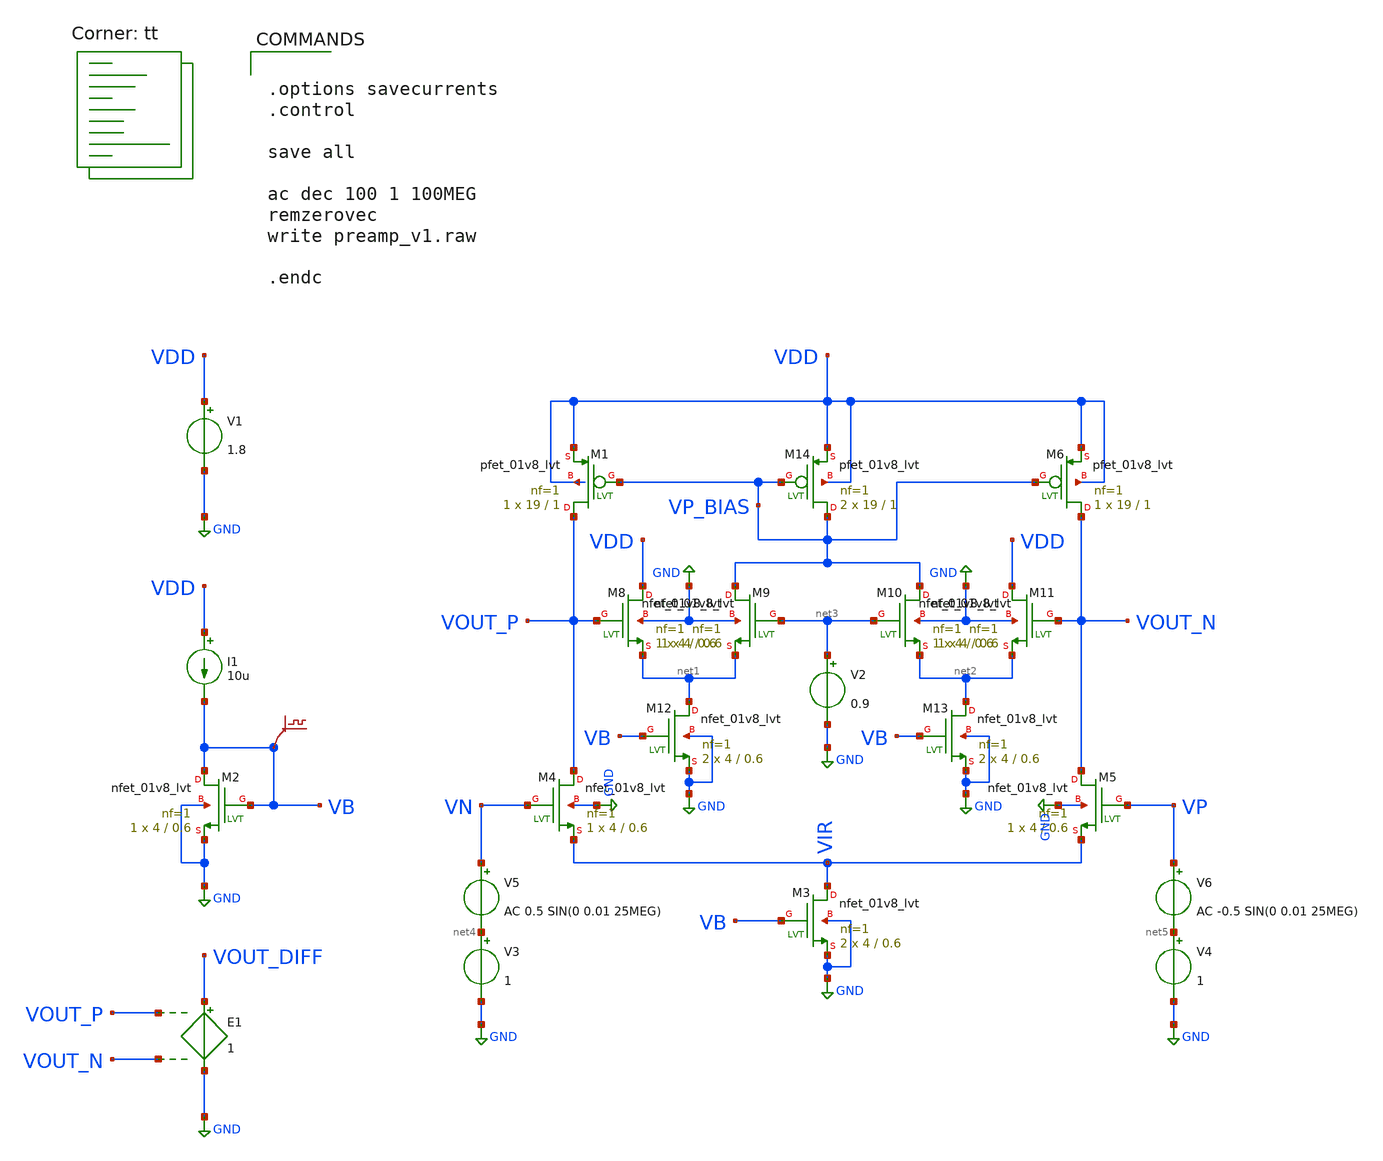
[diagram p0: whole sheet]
** sch_path: strongARM/preamp_v1.sch
**.subckt preamp_v1
V1 VDD GND 1.8
XM2 VB VB GND GND sky130_fd_pr__nfet_01v8_lvt L=0.6 W=4 nf=1 ad='int((nf+1)/2) * W/nf * 0.29' as='int((nf+2)/2) * W/nf * 0.29'
+ pd='2*int((nf+1)/2) * (W/nf + 0.29)' ps='2*int((nf+2)/2) * (W/nf + 0.29)' nrd='0.29 / W' nrs='0.29 / W'
+ sa=0 sb=0 sd=0 mult=1 m=1
I1 VDD VB 10u
XM3 VIR VB GND GND sky130_fd_pr__nfet_01v8_lvt L=0.6 W=4 nf=1 ad='int((nf+1)/2) * W/nf * 0.29' as='int((nf+2)/2) * W/nf * 0.29'
+ pd='2*int((nf+1)/2) * (W/nf + 0.29)' ps='2*int((nf+2)/2) * (W/nf + 0.29)' nrd='0.29 / W' nrs='0.29 / W'
+ sa=0 sb=0 sd=0 mult=2 m=2
XM4 VOUT_P VN VIR GND sky130_fd_pr__nfet_01v8_lvt L=0.6 W=4 nf=1 ad='int((nf+1)/2) * W/nf * 0.29' as='int((nf+2)/2) * W/nf * 0.29'
+ pd='2*int((nf+1)/2) * (W/nf + 0.29)' ps='2*int((nf+2)/2) * (W/nf + 0.29)' nrd='0.29 / W' nrs='0.29 / W'
+ sa=0 sb=0 sd=0 mult=1 m=1
XM5 VOUT_N VP VIR GND sky130_fd_pr__nfet_01v8_lvt L=0.6 W=4 nf=1 ad='int((nf+1)/2) * W/nf * 0.29' as='int((nf+2)/2) * W/nf * 0.29'
+ pd='2*int((nf+1)/2) * (W/nf + 0.29)' ps='2*int((nf+2)/2) * (W/nf + 0.29)' nrd='0.29 / W' nrs='0.29 / W'
+ sa=0 sb=0 sd=0 mult=1 m=1
XM6 VOUT_N VP_BIAS VDD VDD sky130_fd_pr__pfet_01v8_lvt L=1 W=19 nf=1 ad='int((nf+1)/2) * W/nf * 0.29'
+ as='int((nf+2)/2) * W/nf * 0.29' pd='2*int((nf+1)/2) * (W/nf + 0.29)' ps='2*int((nf+2)/2) * (W/nf + 0.29)'
+ nrd='0.29 / W' nrs='0.29 / W' sa=0 sb=0 sd=0 mult=1 m=1
XM8 VDD VOUT_P net1 GND sky130_fd_pr__nfet_01v8_lvt L=0.6 W=4 nf=1 ad='int((nf+1)/2) * W/nf * 0.29' as='int((nf+2)/2) * W/nf * 0.29'
+ pd='2*int((nf+1)/2) * (W/nf + 0.29)' ps='2*int((nf+2)/2) * (W/nf + 0.29)' nrd='0.29 / W' nrs='0.29 / W'
+ sa=0 sb=0 sd=0 mult=1 m=1
XM9 VP_BIAS net3 net1 GND sky130_fd_pr__nfet_01v8_lvt L=0.6 W=4 nf=1 ad='int((nf+1)/2) * W/nf * 0.29'
+ as='int((nf+2)/2) * W/nf * 0.29' pd='2*int((nf+1)/2) * (W/nf + 0.29)' ps='2*int((nf+2)/2) * (W/nf + 0.29)'
+ nrd='0.29 / W' nrs='0.29 / W' sa=0 sb=0 sd=0 mult=1 m=1
XM10 VP_BIAS net3 net2 GND sky130_fd_pr__nfet_01v8_lvt L=0.6 W=4 nf=1 ad='int((nf+1)/2) * W/nf * 0.29'
+ as='int((nf+2)/2) * W/nf * 0.29' pd='2*int((nf+1)/2) * (W/nf + 0.29)' ps='2*int((nf+2)/2) * (W/nf + 0.29)'
+ nrd='0.29 / W' nrs='0.29 / W' sa=0 sb=0 sd=0 mult=1 m=1
XM11 VDD VOUT_N net2 GND sky130_fd_pr__nfet_01v8_lvt L=0.6 W=4 nf=1 ad='int((nf+1)/2) * W/nf * 0.29'
+ as='int((nf+2)/2) * W/nf * 0.29' pd='2*int((nf+1)/2) * (W/nf + 0.29)' ps='2*int((nf+2)/2) * (W/nf + 0.29)'
+ nrd='0.29 / W' nrs='0.29 / W' sa=0 sb=0 sd=0 mult=1 m=1
XM12 net1 VB GND GND sky130_fd_pr__nfet_01v8_lvt L=0.6 W=4 nf=1 ad='int((nf+1)/2) * W/nf * 0.29' as='int((nf+2)/2) * W/nf * 0.29'
+ pd='2*int((nf+1)/2) * (W/nf + 0.29)' ps='2*int((nf+2)/2) * (W/nf + 0.29)' nrd='0.29 / W' nrs='0.29 / W'
+ sa=0 sb=0 sd=0 mult=2 m=2
XM13 net2 VB GND GND sky130_fd_pr__nfet_01v8_lvt L=0.6 W=4 nf=1 ad='int((nf+1)/2) * W/nf * 0.29' as='int((nf+2)/2) * W/nf * 0.29'
+ pd='2*int((nf+1)/2) * (W/nf + 0.29)' ps='2*int((nf+2)/2) * (W/nf + 0.29)' nrd='0.29 / W' nrs='0.29 / W'
+ sa=0 sb=0 sd=0 mult=2 m=2
XM14 VP_BIAS VP_BIAS VDD VDD sky130_fd_pr__pfet_01v8_lvt L=1 W=19 nf=1 ad='int((nf+1)/2) * W/nf * 0.29'
+ as='int((nf+2)/2) * W/nf * 0.29' pd='2*int((nf+1)/2) * (W/nf + 0.29)' ps='2*int((nf+2)/2) * (W/nf + 0.29)'
+ nrd='0.29 / W' nrs='0.29 / W' sa=0 sb=0 sd=0 mult=2 m=2
V2 net3 GND 0.9
.save v(vb)
V3 net4 GND 1
V4 net5 GND 1
XM1 VOUT_P VP_BIAS VDD VDD sky130_fd_pr__pfet_01v8_lvt L=1 W=19 nf=1 ad='int((nf+1)/2) * W/nf * 0.29'
+ as='int((nf+2)/2) * W/nf * 0.29' pd='2*int((nf+1)/2) * (W/nf + 0.29)' ps='2*int((nf+2)/2) * (W/nf + 0.29)'
+ nrd='0.29 / W' nrs='0.29 / W' sa=0 sb=0 sd=0 mult=1 m=1
V5 VN net4 AC 0.5 SIN(0 0.01 25MEG)
V6 VP net5 AC -0.5 SIN(0 0.01 25MEG)
E1 VOUT_DIFF GND VOUT_P VOUT_N 1
**** begin user architecture code
.lib $::SKYWATER_MODELS/sky130.lib.spice tt


.options savecurrents
.control

save all

ac dec 100 1 100MEG
remzerovec
write preamp_v1.raw

.endc


**** end user architecture code
**.ends
.GLOBAL GND
.end
